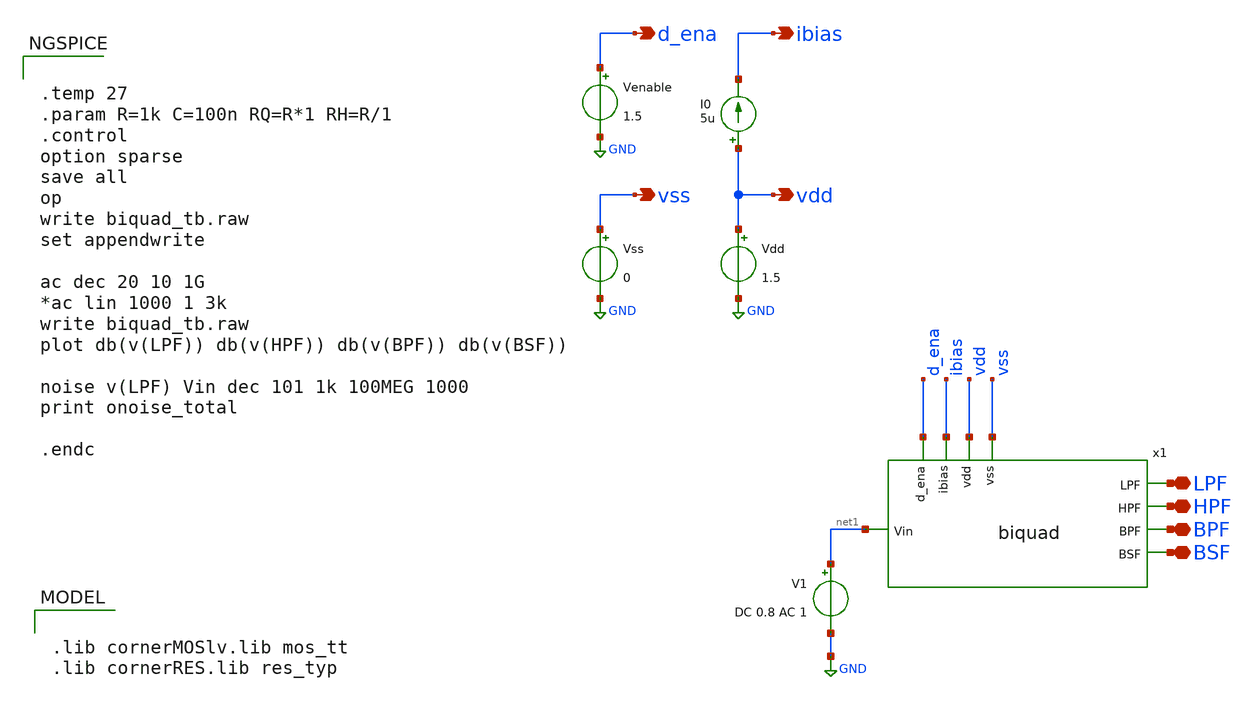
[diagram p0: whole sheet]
** sch_path: prj/template/3_Real_circuits/biquad_tb.sch
**.subckt biquad_tb vss vdd ibias d_ena LPF HPF BPF BSF
*.opin vss
*.opin vdd
*.opin ibias
*.opin d_ena
*.iopin LPF
*.iopin HPF
*.iopin BPF
*.iopin BSF
V1 net1 GND DC 0.8 AC 1
Vss vss GND 0
Vdd vdd GND 1.5
I0 vdd ibias 5u
Venable d_ena GND 1.5
x1 BPF LPF vdd ibias HPF vss d_ena BSF net1 biquad
**** begin user architecture code


.temp 27
.param R=1k C=100n RQ=R*1 RH=R/1
.control
option sparse
save all
op
write biquad_tb.raw
set appendwrite

ac dec 20 10 1G
*ac lin 1000 1 3k
write biquad_tb.raw
plot db(v(LPF)) db(v(HPF)) db(v(BPF)) db(v(BSF))

noise v(LPF) Vin dec 101 1k 100MEG 1000
print onoise_total

.endc



.lib cornerMOSlv.lib mos_tt
.lib cornerRES.lib res_typ

**** end user architecture code
**.ends
.GLOBAL GND
.end
